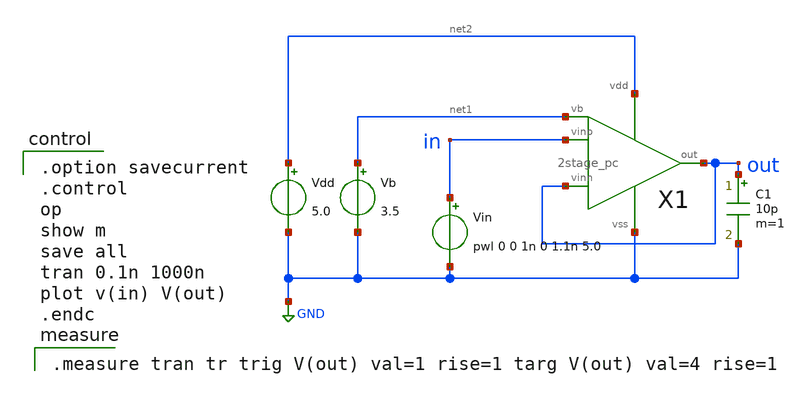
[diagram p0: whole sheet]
** sch_path: OR1/PTC06/opamp/2stage_pc_tran.sch
**.subckt 2stage_pc_tran
Vdd net2 GND 5.0
Vb net1 GND 3.5
C1 out GND 10p m=1
Vin in GND pwl 0 0 1n 0 1.1n 5.0
X1 in out net1 out net2 GND 2stage_pc
**** begin user architecture code

.option savecurrent
.control
op
show m
save all
tran 0.1n 1000n
plot v(in) V(out)
.endc


.measure tran tr trig V(out) val=1 rise=1 targ V(out) val=4 rise=1

 .include $::LIB/mos.lib
.include $::LIB/passive.lib
.include $::LIB/diode.lib
**** end user architecture code
**.ends

* expanding   symbol:  2stage_pc.sym # of pins=6
** sym_path: 2stage_pc.sym
** sch_path: 2stage_pc.sch
.subckt 2stage_pc vinp vinn vb out vdd vss
*.ipin vinp
*.ipin vinn
*.ipin vb
*.opin out
*.iopin vdd
*.iopin vss
X1 vinp vinn net2 vdd vss vb diff
X2 net2 vb out vdd vss cs
M2 net3 net1 net2 vss nmos L=2u W=40u m=1
M6 net1 vb vdd vdd pmos L=2u W=20u m=1
M1 net1 net1 net4 vss nmos L=2u W=10u m=1
M7 net4 net4 vss vss nmos L=2u W=10u m=1
C1 out net3 poly_cap W=18 L=18
.ends


* expanding   symbol:  diff.sym # of pins=6
** sym_path: diff.sym
** sch_path: diff.sch
.subckt diff vinp vinn out vdd vss vb
*.ipin vinn
*.ipin vinp
*.ipin vb
*.opin out
*.iopin vdd
*.iopin vss
M5 net2 vb vdd vdd pmos L=2u W=40u m=1
M1 net1 vinn net2 net2 pmos L=2u W=200u m=1
M2 out vinp net2 net2 pmos L=2u W=200u m=1
M3 net1 net1 vss vss nmos L=2u W=10u m=1
M4 out net1 vss vss nmos L=2u W=10u m=1
.ends


* expanding   symbol:  cs.sym # of pins=5
** sym_path: cs.sym
** sch_path: cs.sch
.subckt cs vin vb out vdd vss
*.ipin vb
*.ipin vin
*.opin out
*.iopin vss
*.iopin vdd
M6 out vb vdd vdd pmos L=2u W=400u m=1
M7 out vin vss vss nmos L=2u W=200u m=1
.ends

.GLOBAL GND
.end
